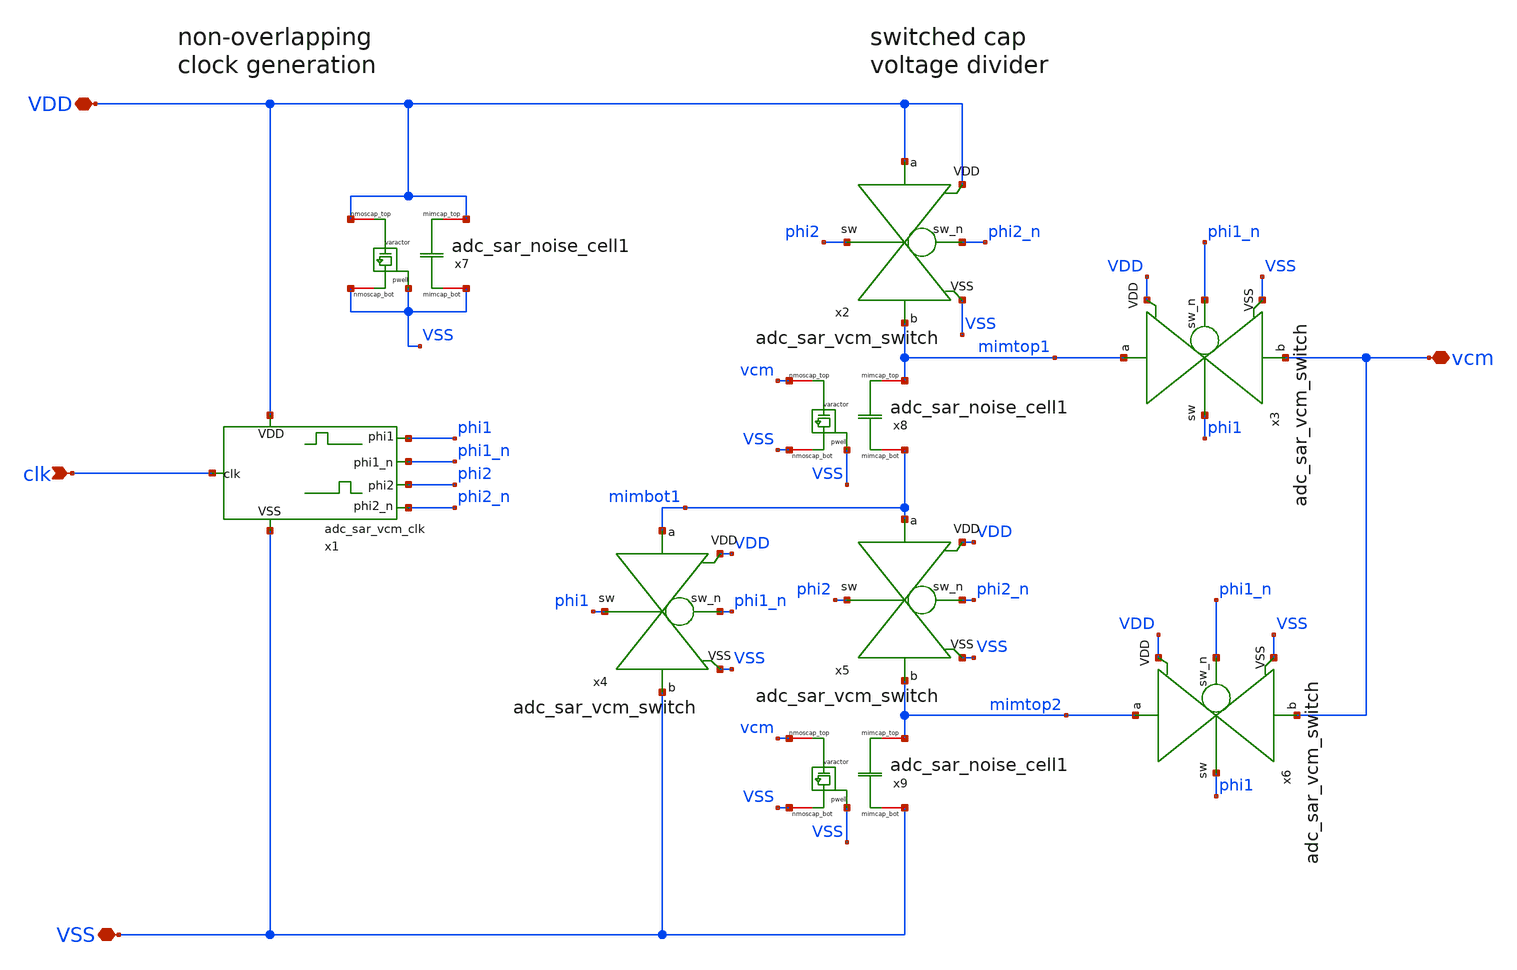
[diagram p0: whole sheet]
** sch_path: adc_sar_vcm_generator.sch
**.subckt adc_sar_vcm_generator VDD VSS clk vcm
*.iopin VDD
*.iopin VSS
*.ipin clk
*.iopin vcm
x1 VDD VSS phi1_n phi1 phi2 phi2_n clk adc_sar_vcm_clk
x2 phi2_n VDD phi2 mimtop1 VDD VSS adc_sar_vcm_switch
x3 phi1_n mimtop1 phi1 vcm VDD VSS adc_sar_vcm_switch
x4 phi1_n mimbot1 phi1 VSS VDD VSS adc_sar_vcm_switch
x5 phi2_n mimbot1 phi2 mimtop2 VDD VSS adc_sar_vcm_switch
x6 phi1_n mimtop2 phi1 vcm VDD VSS adc_sar_vcm_switch
x7 VDD VSS VDD VSS VSS adc_sar_noise_cell1
x8 mimtop1 mimbot1 vcm VSS VSS adc_sar_noise_cell1
x9 mimtop2 VSS vcm VSS VSS adc_sar_noise_cell1
**.ends
.end
